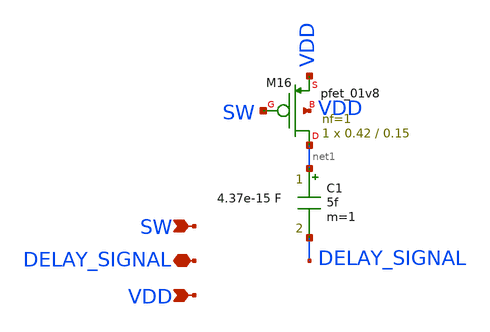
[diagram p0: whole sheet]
** sch_path: hgu/xschem/hgu_sw_cap_pmos.sch
**.subckt hgu_sw_cap_pmos SW VDD DELAY_SIGNAL
*.ipin SW
*.ipin VDD
*.iopin DELAY_SIGNAL
XM16 net1 SW VDD VDD sky130_fd_pr__pfet_01v8 L=0.15 W=0.42 nf=1 ad='int((nf+1)/2) * W/nf * 0.29' as='int((nf+2)/2) * W/nf * 0.29'
+ pd='2*int((nf+1)/2) * (W/nf + 0.29)' ps='2*int((nf+2)/2) * (W/nf + 0.29)' nrd='0.29 / W' nrs='0.29 / W'
+ sa=0 sb=0 sd=0 mult=1 m=1
C1 net1 DELAY_SIGNAL 5f m=1
**.ends
.end
